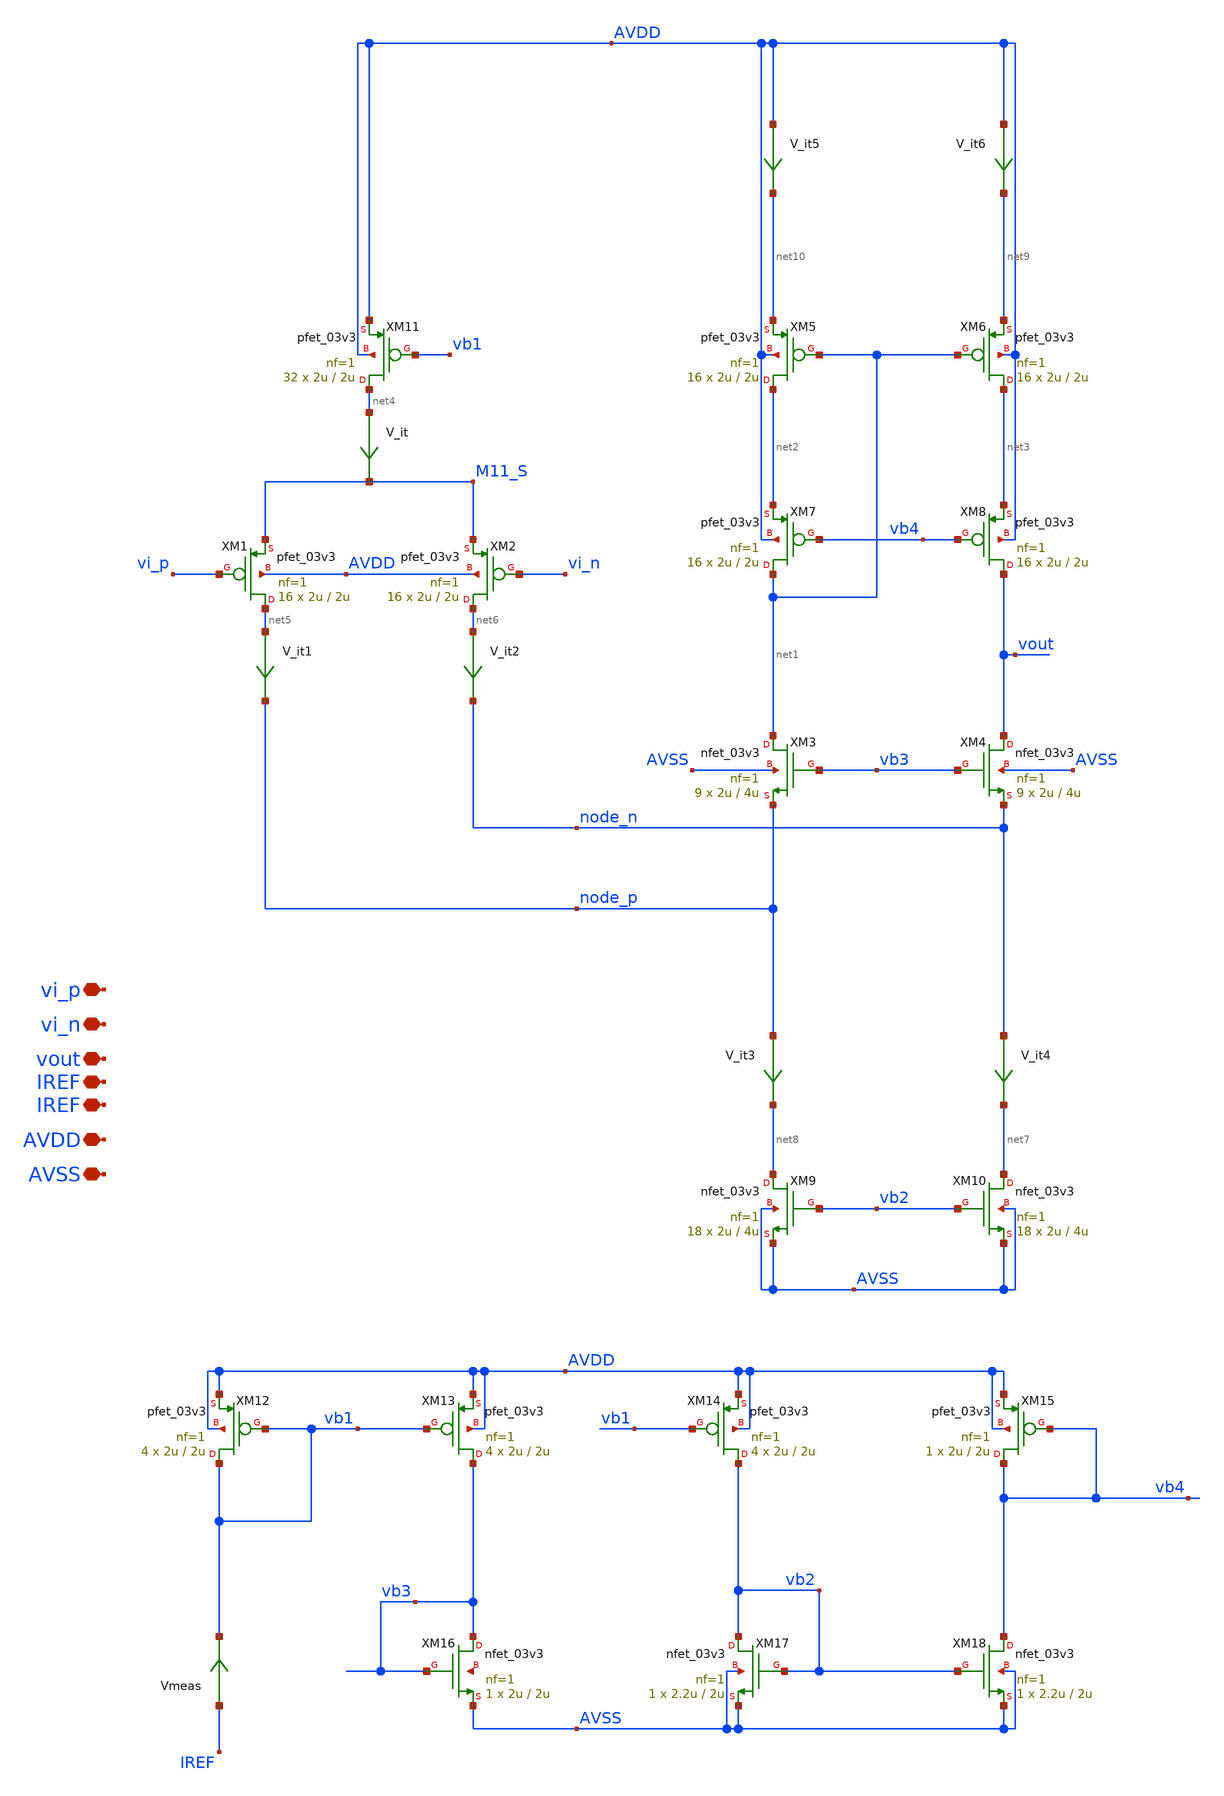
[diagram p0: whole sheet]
** sch_path: TIA/Folded/FoldedCascode.sch
**.subckt FoldedCascode AVDD AVSS IREF vout vi_p vi_n IREF
*.iopin AVDD
*.iopin AVSS
*.iopin IREF
*.iopin vout
*.iopin vi_p
*.iopin vi_n
*.iopin IREF
XM3 net1 vb3 node_p AVSS nfet_03v3 L=4u W=2u nf=1 ad='int((nf+1)/2) * W/nf * 0.18u' as='int((nf+2)/2) * W/nf * 0.18u'
+ pd='2*int((nf+1)/2) * (W/nf + 0.18u)' ps='2*int((nf+2)/2) * (W/nf + 0.18u)' nrd='0.18u / W' nrs='0.18u / W'
+ sa=0 sb=0 sd=0 m=9
XM1 net5 vi_p M11_S AVDD pfet_03v3 L=2u W=2u nf=1 ad='int((nf+1)/2) * W/nf * 0.18u' as='int((nf+2)/2) * W/nf * 0.18u'
+ pd='2*int((nf+1)/2) * (W/nf + 0.18u)' ps='2*int((nf+2)/2) * (W/nf + 0.18u)' nrd='0.18u / W' nrs='0.18u / W'
+ sa=0 sb=0 sd=0 m=16
XM2 net6 vi_n M11_S AVDD pfet_03v3 L=2u W=2u nf=1 ad='int((nf+1)/2) * W/nf * 0.18u' as='int((nf+2)/2) * W/nf * 0.18u'
+ pd='2*int((nf+1)/2) * (W/nf + 0.18u)' ps='2*int((nf+2)/2) * (W/nf + 0.18u)' nrd='0.18u / W' nrs='0.18u / W'
+ sa=0 sb=0 sd=0 m=16
XM4 vout vb3 node_n AVSS nfet_03v3 L=4u W=2u nf=1 ad='int((nf+1)/2) * W/nf * 0.18u' as='int((nf+2)/2) * W/nf * 0.18u'
+ pd='2*int((nf+1)/2) * (W/nf + 0.18u)' ps='2*int((nf+2)/2) * (W/nf + 0.18u)' nrd='0.18u / W' nrs='0.18u / W'
+ sa=0 sb=0 sd=0 m=9
XM5 net2 net1 net10 AVDD pfet_03v3 L=2u W=2u nf=1 ad='int((nf+1)/2) * W/nf * 0.18u' as='int((nf+2)/2) * W/nf * 0.18u'
+ pd='2*int((nf+1)/2) * (W/nf + 0.18u)' ps='2*int((nf+2)/2) * (W/nf + 0.18u)' nrd='0.18u / W' nrs='0.18u / W'
+ sa=0 sb=0 sd=0 m=16
XM6 net3 net1 net9 AVDD pfet_03v3 L=2u W=2u nf=1 ad='int((nf+1)/2) * W/nf * 0.18u' as='int((nf+2)/2) * W/nf * 0.18u'
+ pd='2*int((nf+1)/2) * (W/nf + 0.18u)' ps='2*int((nf+2)/2) * (W/nf + 0.18u)' nrd='0.18u / W' nrs='0.18u / W'
+ sa=0 sb=0 sd=0 m=16
XM7 net1 vb4 net2 AVDD pfet_03v3 L=2u W=2u nf=1 ad='int((nf+1)/2) * W/nf * 0.18u' as='int((nf+2)/2) * W/nf * 0.18u'
+ pd='2*int((nf+1)/2) * (W/nf + 0.18u)' ps='2*int((nf+2)/2) * (W/nf + 0.18u)' nrd='0.18u / W' nrs='0.18u / W'
+ sa=0 sb=0 sd=0 m=16
XM8 vout vb4 net3 AVDD pfet_03v3 L=2u W=2u nf=1 ad='int((nf+1)/2) * W/nf * 0.18u' as='int((nf+2)/2) * W/nf * 0.18u'
+ pd='2*int((nf+1)/2) * (W/nf + 0.18u)' ps='2*int((nf+2)/2) * (W/nf + 0.18u)' nrd='0.18u / W' nrs='0.18u / W'
+ sa=0 sb=0 sd=0 m=16
XM9 net8 vb2 AVSS AVSS nfet_03v3 L=4u W=2u nf=1 ad='int((nf+1)/2) * W/nf * 0.18u' as='int((nf+2)/2) * W/nf * 0.18u'
+ pd='2*int((nf+1)/2) * (W/nf + 0.18u)' ps='2*int((nf+2)/2) * (W/nf + 0.18u)' nrd='0.18u / W' nrs='0.18u / W'
+ sa=0 sb=0 sd=0 m=18
XM10 net7 vb2 AVSS AVSS nfet_03v3 L=4u W=2u nf=1 ad='int((nf+1)/2) * W/nf * 0.18u' as='int((nf+2)/2) * W/nf * 0.18u'
+ pd='2*int((nf+1)/2) * (W/nf + 0.18u)' ps='2*int((nf+2)/2) * (W/nf + 0.18u)' nrd='0.18u / W' nrs='0.18u / W'
+ sa=0 sb=0 sd=0 m=18
XM11 net4 vb1 AVDD AVDD pfet_03v3 L=2u W=2u nf=1 ad='int((nf+1)/2) * W/nf * 0.18u' as='int((nf+2)/2) * W/nf * 0.18u'
+ pd='2*int((nf+1)/2) * (W/nf + 0.18u)' ps='2*int((nf+2)/2) * (W/nf + 0.18u)' nrd='0.18u / W' nrs='0.18u / W'
+ sa=0 sb=0 sd=0 m=32
V_it1 net5 node_p 0
.save i(v_it1)
V_it2 net6 node_n 0
.save i(v_it2)
V_it net4 M11_S 0
.save i(v_it)
V_it3 node_p net8 0
.save i(v_it3)
V_it4 node_n net7 0
.save i(v_it4)
V_it5 AVDD net10 0
.save i(v_it5)
V_it6 AVDD net9 0
.save i(v_it6)
XM16 vb3 vb3 AVSS net11 nfet_03v3 L=2u W=2u nf=1 ad='int((nf+1)/2) * W/nf * 0.18u' as='int((nf+2)/2) * W/nf * 0.18u'
+ pd='2*int((nf+1)/2) * (W/nf + 0.18u)' ps='2*int((nf+2)/2) * (W/nf + 0.18u)' nrd='0.18u / W' nrs='0.18u / W'
+ sa=0 sb=0 sd=0 m=1
XM12 vb1 vb1 AVDD AVDD pfet_03v3 L=2u W=2u nf=1 ad='int((nf+1)/2) * W/nf * 0.18u' as='int((nf+2)/2) * W/nf * 0.18u'
+ pd='2*int((nf+1)/2) * (W/nf + 0.18u)' ps='2*int((nf+2)/2) * (W/nf + 0.18u)' nrd='0.18u / W' nrs='0.18u / W'
+ sa=0 sb=0 sd=0 m=4
XM13 vb3 vb1 AVDD AVDD pfet_03v3 L=2u W=2u nf=1 ad='int((nf+1)/2) * W/nf * 0.18u' as='int((nf+2)/2) * W/nf * 0.18u'
+ pd='2*int((nf+1)/2) * (W/nf + 0.18u)' ps='2*int((nf+2)/2) * (W/nf + 0.18u)' nrd='0.18u / W' nrs='0.18u / W'
+ sa=0 sb=0 sd=0 m=4
XM14 vb2 vb1 AVDD AVDD pfet_03v3 L=2u W=2u nf=1 ad='int((nf+1)/2) * W/nf * 0.18u' as='int((nf+2)/2) * W/nf * 0.18u'
+ pd='2*int((nf+1)/2) * (W/nf + 0.18u)' ps='2*int((nf+2)/2) * (W/nf + 0.18u)' nrd='0.18u / W' nrs='0.18u / W'
+ sa=0 sb=0 sd=0 m=4
XM15 vb4 vb4 AVDD AVDD pfet_03v3 L=2u W=2u nf=1 ad='int((nf+1)/2) * W/nf * 0.18u' as='int((nf+2)/2) * W/nf * 0.18u'
+ pd='2*int((nf+1)/2) * (W/nf + 0.18u)' ps='2*int((nf+2)/2) * (W/nf + 0.18u)' nrd='0.18u / W' nrs='0.18u / W'
+ sa=0 sb=0 sd=0 m=1
XM17 vb2 vb2 AVSS AVSS nfet_03v3 L=2u W=2.2u nf=1 ad='int((nf+1)/2) * W/nf * 0.18u' as='int((nf+2)/2) * W/nf * 0.18u'
+ pd='2*int((nf+1)/2) * (W/nf + 0.18u)' ps='2*int((nf+2)/2) * (W/nf + 0.18u)' nrd='0.18u / W' nrs='0.18u / W'
+ sa=0 sb=0 sd=0 m=1
XM18 vb4 vb2 AVSS AVSS nfet_03v3 L=2u W=2.2u nf=1 ad='int((nf+1)/2) * W/nf * 0.18u' as='int((nf+2)/2) * W/nf * 0.18u'
+ pd='2*int((nf+1)/2) * (W/nf + 0.18u)' ps='2*int((nf+2)/2) * (W/nf + 0.18u)' nrd='0.18u / W' nrs='0.18u / W'
+ sa=0 sb=0 sd=0 m=1
Vmeas IREF vb1 0
.save i(vmeas)
**.ends
.end
